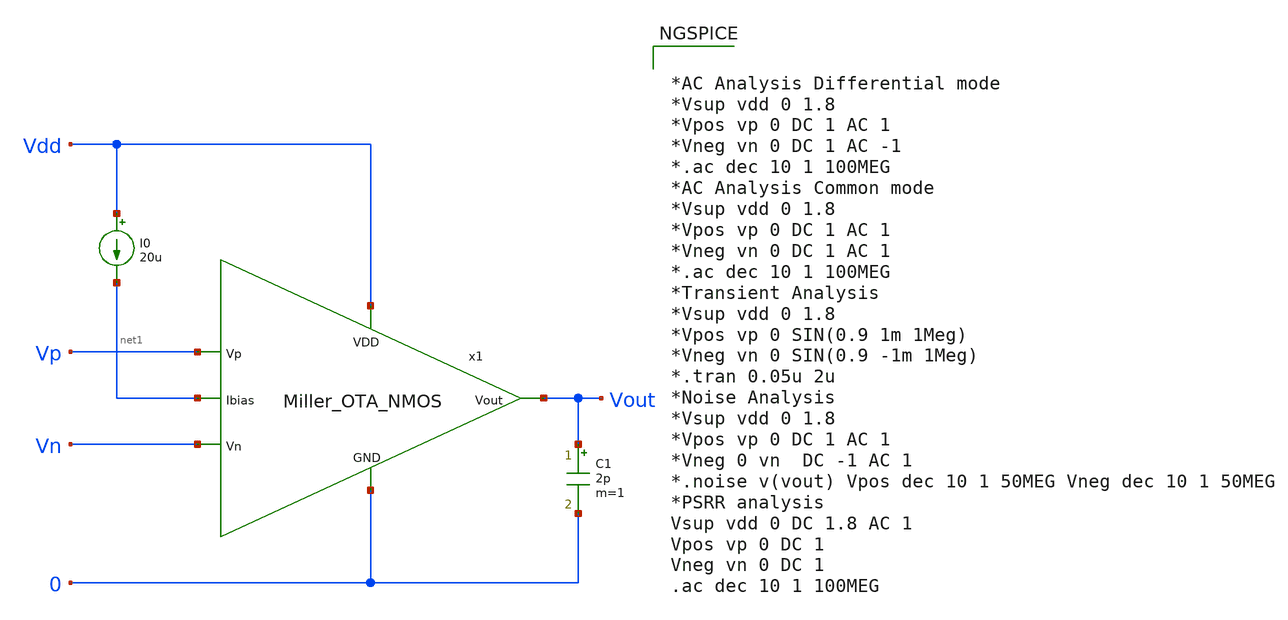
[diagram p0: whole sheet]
** sch_path: Analog_Blocks/OTA/Testbench/Miller_OTA_NMOS_TB.sch
**.subckt Miller_OTA_NMOS_TB
I0 Vdd net1 20u
C1 Vout 0 2p m=1
x1 Vdd Vn Vp Vout net1 0 Miller_OTA_NMOS
**** begin user architecture code


*AC Analysis Differential mode
*Vsup vdd 0 1.8
*Vpos vp 0 DC 1 AC 1
*Vneg vn 0 DC 1 AC -1
*.ac dec 10 1 100MEG
*AC Analysis Common mode
*Vsup vdd 0 1.8
*Vpos vp 0 DC 1 AC 1
*Vneg vn 0 DC 1 AC 1
*.ac dec 10 1 100MEG
*Transient Analysis
*Vsup vdd 0 1.8
*Vpos vp 0 SIN(0.9 1m 1Meg)
*Vneg vn 0 SIN(0.9 -1m 1Meg)
*.tran 0.05u 2u
*Noise Analysis
*Vsup vdd 0 1.8
*Vpos vp 0 DC 1 AC 1
*Vneg 0 vn  DC -1 AC 1
*.noise v(vout) Vpos dec 10 1 50MEG Vneg dec 10 1 50MEG
*PSRR analysis
Vsup vdd 0 DC 1.8 AC 1
Vpos vp 0 DC 1
Vneg vn 0 DC 1
.ac dec 10 1 100MEG



.include $::SKYWATER_MODELS/cells/nfet_01v8/sky130_fd_pr__nfet_01v8__tt.corner.spice
.include $::SKYWATER_MODELS/cells/nfet_01v8_lvt/sky130_fd_pr__nfet_01v8_lvt__tt.corner.spice
.include $::SKYWATER_MODELS/cells/pfet_01v8/sky130_fd_pr__pfet_01v8__tt.corner.spice
.include $::SKYWATER_MODELS/cells/nfet_03v3_nvt/sky130_fd_pr__nfet_03v3_nvt__tt.corner.spice
.include $::SKYWATER_MODELS/cells/nfet_05v0_nvt/sky130_fd_pr__nfet_05v0_nvt__tt.corner.spice
.include $::SKYWATER_MODELS/cells/esd_nfet_01v8/sky130_fd_pr__esd_nfet_01v8__tt.corner.spice
.include $::SKYWATER_MODELS/cells/pfet_01v8_lvt/sky130_fd_pr__pfet_01v8_lvt__tt.corner.spice
.include $::SKYWATER_MODELS/cells/pfet_01v8_hvt/sky130_fd_pr__pfet_01v8_hvt__tt.corner.spice
.include $::SKYWATER_MODELS/cells/esd_pfet_g5v0d10v5/sky130_fd_pr__esd_pfet_g5v0d10v5__tt.corner.spice
.include $::SKYWATER_MODELS/cells/pfet_g5v0d10v5/sky130_fd_pr__pfet_g5v0d10v5__tt.corner.spice
.include $::SKYWATER_MODELS/cells/pfet_g5v0d16v0/sky130_fd_pr__pfet_g5v0d16v0__tt.corner.spice
.include $::SKYWATER_MODELS/cells/nfet_g5v0d10v5/sky130_fd_pr__nfet_g5v0d10v5__tt.corner.spice
.include $::SKYWATER_MODELS/cells/nfet_g5v0d16v0/sky130_fd_pr__nfet_g5v0d16v0__tt_discrete.corner.spice
.include $::SKYWATER_MODELS/cells/esd_nfet_g5v0d10v5/sky130_fd_pr__esd_nfet_g5v0d10v5__tt.corner.spice
.include $::SKYWATER_MODELS/models/corners/tt/nonfet.spice
* Mismatch parameters
.include $::SKYWATER_MODELS/cells/nfet_01v8/sky130_fd_pr__nfet_01v8__mismatch.corner.spice
.include $::SKYWATER_MODELS/cells/pfet_01v8/sky130_fd_pr__pfet_01v8__mismatch.corner.spice
.include $::SKYWATER_MODELS/cells/nfet_01v8_lvt/sky130_fd_pr__nfet_01v8_lvt__mismatch.corner.spice
.include $::SKYWATER_MODELS/cells/pfet_01v8_lvt/sky130_fd_pr__pfet_01v8_lvt__mismatch.corner.spice
.include $::SKYWATER_MODELS/cells/pfet_01v8_hvt/sky130_fd_pr__pfet_01v8_hvt__mismatch.corner.spice
.include $::SKYWATER_MODELS/cells/nfet_g5v0d10v5/sky130_fd_pr__nfet_g5v0d10v5__mismatch.corner.spice
.include $::SKYWATER_MODELS/cells/pfet_g5v0d10v5/sky130_fd_pr__pfet_g5v0d10v5__mismatch.corner.spice
.include $::SKYWATER_MODELS/cells/nfet_05v0_nvt/sky130_fd_pr__nfet_05v0_nvt__mismatch.corner.spice
.include $::SKYWATER_MODELS/cells/nfet_03v3_nvt/sky130_fd_pr__nfet_03v3_nvt__mismatch.corner.spice
* Resistor$::SKYWATER_MODELS/Capacitor
.include $::SKYWATER_MODELS/models/r+c/res_typical__cap_typical.spice
.include $::SKYWATER_MODELS/models/r+c/res_typical__cap_typical__lin.spice
* Special cells
.include $::SKYWATER_MODELS/models/corners/tt/specialized_cells.spice
* All models
.include $::SKYWATER_MODELS/models/all.spice
* Corner
.include $::SKYWATER_MODELS/models/corners/tt/rf.spice

**** end user architecture code
**.ends

* expanding   symbol:
*+  /home/eslam/Analog_Design/Analog_Blocks/OTA/Schematic/Miller_OTA/Transistor5v/Miller_OTA_NMOS.sym # of pins=6
** sym_path: Analog_Blocks/OTA/Schematic/Miller_OTA/Transistor5v/Miller_OTA_NMOS.sym
** sch_path: Analog_Blocks/OTA/Schematic/Miller_OTA/Transistor5v/Miller_OTA_NMOS.sch
.subckt Miller_OTA_NMOS VDD Vn Vp Vout Ibias GND
*.ipin VDD
*.ipin Ibias
*.ipin Vn
*.ipin Vp
*.opin Vout
*.ipin GND
XM1 net1 Vn net3 GND sky130_fd_pr__nfet_g5v0d10v5 L=0.5 W=10 nf=1 ad='int((nf+1)/2) * W/nf * 0.29' as='int((nf+2)/2) * W/nf * 0.29'
+ pd='2*int((nf+1)/2) * (W/nf + 0.29)' ps='2*int((nf+2)/2) * (W/nf + 0.29)' nrd='0.29 / W' nrs='0.29 / W'
+ sa=0 sb=0 sd=0 mult=8 m=8
XM2 net2 Vp net3 GND sky130_fd_pr__nfet_g5v0d10v5 L=0.5 W=10 nf=1 ad='int((nf+1)/2) * W/nf * 0.29' as='int((nf+2)/2) * W/nf * 0.29'
+ pd='2*int((nf+1)/2) * (W/nf + 0.29)' ps='2*int((nf+2)/2) * (W/nf + 0.29)' nrd='0.29 / W' nrs='0.29 / W'
+ sa=0 sb=0 sd=0 mult=8 m=8
XM3 net1 net1 VDD VDD sky130_fd_pr__pfet_g5v0d10v5 L=0.5 W=5 nf=1 ad='int((nf+1)/2) * W/nf * 0.29' as='int((nf+2)/2) * W/nf * 0.29'
+ pd='2*int((nf+1)/2) * (W/nf + 0.29)' ps='2*int((nf+2)/2) * (W/nf + 0.29)' nrd='0.29 / W' nrs='0.29 / W'
+ sa=0 sb=0 sd=0 mult=4 m=4
XM4 net2 net1 VDD VDD sky130_fd_pr__pfet_g5v0d10v5 L=0.5 W=5 nf=1 ad='int((nf+1)/2) * W/nf * 0.29' as='int((nf+2)/2) * W/nf * 0.29'
+ pd='2*int((nf+1)/2) * (W/nf + 0.29)' ps='2*int((nf+2)/2) * (W/nf + 0.29)' nrd='0.29 / W' nrs='0.29 / W'
+ sa=0 sb=0 sd=0 mult=4 m=4
XM6 Vout net2 VDD VDD sky130_fd_pr__pfet_g5v0d10v5 L=0.5 W=5 nf=1 ad='int((nf+1)/2) * W/nf * 0.29' as='int((nf+2)/2) * W/nf * 0.29'
+ pd='2*int((nf+1)/2) * (W/nf + 0.29)' ps='2*int((nf+2)/2) * (W/nf + 0.29)' nrd='0.29 / W' nrs='0.29 / W'
+ sa=0 sb=0 sd=0 mult=20 m=20
XM5 net3 Ibias GND GND sky130_fd_pr__nfet_g5v0d10v5 L=1 W=3 nf=1 ad='int((nf+1)/2) * W/nf * 0.29' as='int((nf+2)/2) * W/nf * 0.29'
+ pd='2*int((nf+1)/2) * (W/nf + 0.29)' ps='2*int((nf+2)/2) * (W/nf + 0.29)' nrd='0.29 / W' nrs='0.29 / W'
+ sa=0 sb=0 sd=0 mult=8 m=8
XM8 Ibias Ibias GND GND sky130_fd_pr__nfet_g5v0d10v5 L=1 W=3 nf=1 ad='int((nf+1)/2) * W/nf * 0.29' as='int((nf+2)/2) * W/nf * 0.29'
+ pd='2*int((nf+1)/2) * (W/nf + 0.29)' ps='2*int((nf+2)/2) * (W/nf + 0.29)' nrd='0.29 / W' nrs='0.29 / W'
+ sa=0 sb=0 sd=0 mult=8 m=8
XC1 net2 Vout sky130_fd_pr__cap_mim_m3_2 W=25 L=25 MF=1 m=1
XM7 Vout Ibias GND GND sky130_fd_pr__nfet_g5v0d10v5 L=1 W=3 nf=1 ad='int((nf+1)/2) * W/nf * 0.29' as='int((nf+2)/2) * W/nf * 0.29'
+ pd='2*int((nf+1)/2) * (W/nf + 0.29)' ps='2*int((nf+2)/2) * (W/nf + 0.29)' nrd='0.29 / W' nrs='0.29 / W'
+ sa=0 sb=0 sd=0 mult=16 m=16
.ends

.end
